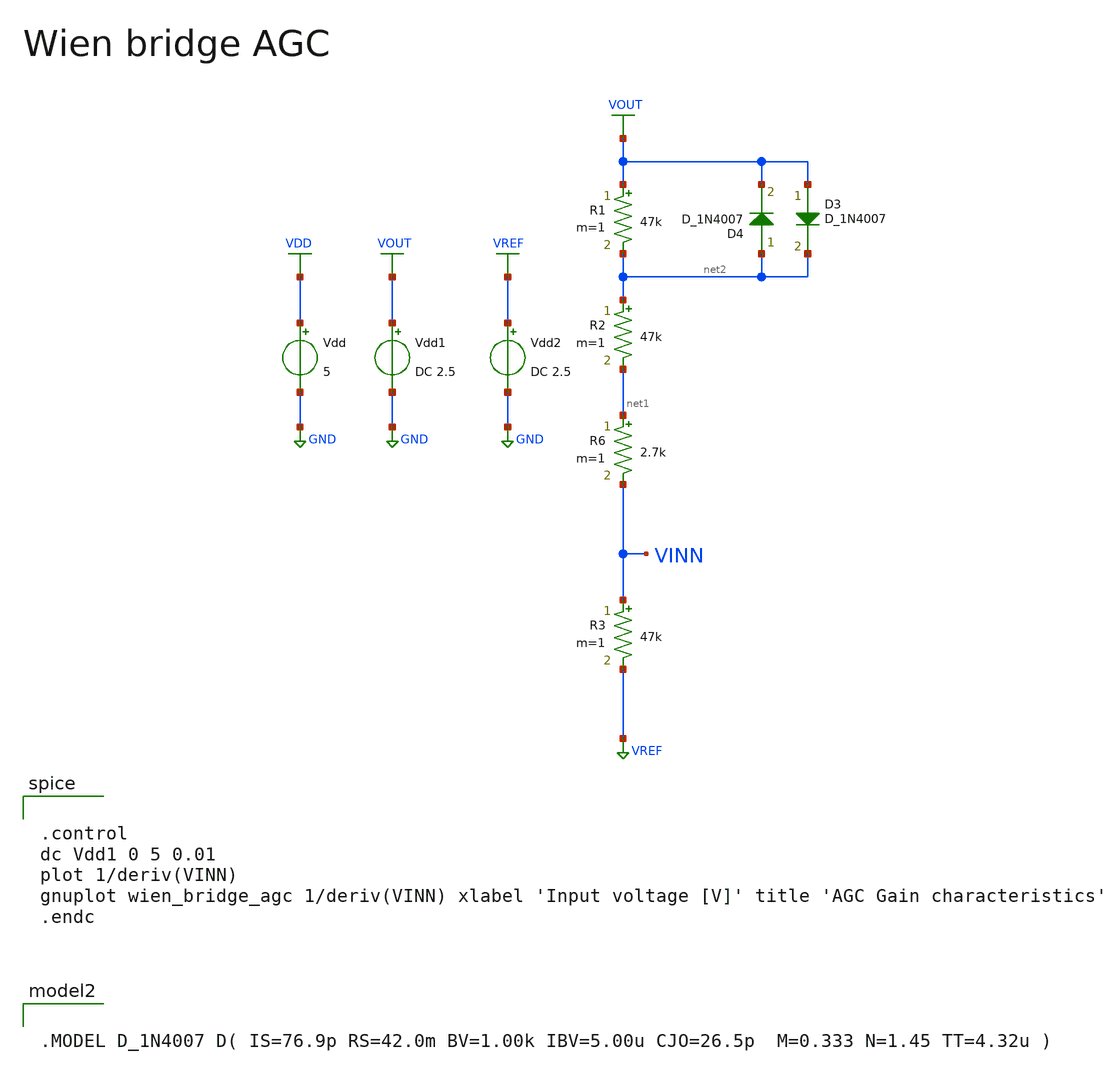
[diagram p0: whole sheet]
** sch_path: Vol.2/files/08/xschem/tb_wien_bridge_agc.sch
**.subckt tb_wien_bridge_agc
Vdd VDD GND 5
Vdd1 VOUT GND DC 2.5
R1 VOUT net2 47k m=1
R2 net2 net1 47k m=1
R3 VINN VREF 47k m=1
Vdd2 VREF GND DC 2.5
R6 net1 VINN 2.7k m=1
D3 VOUT net2 D_1N4007 area=1
D4 net2 VOUT D_1N4007 area=1
**** begin user architecture code


.control
dc Vdd1 0 5 0.01
plot 1/deriv(VINN)
gnuplot wien_bridge_agc 1/deriv(VINN) xlabel 'Input voltage [V]' title 'AGC Gain characteristics'
.endc




.MODEL D_1N4007 D( IS=76.9p RS=42.0m BV=1.00k IBV=5.00u CJO=26.5p  M=0.333 N=1.45 TT=4.32u )


**** end user architecture code
**.ends
.GLOBAL VDD
.GLOBAL GND
.GLOBAL VOUT
.GLOBAL VREF
.end
